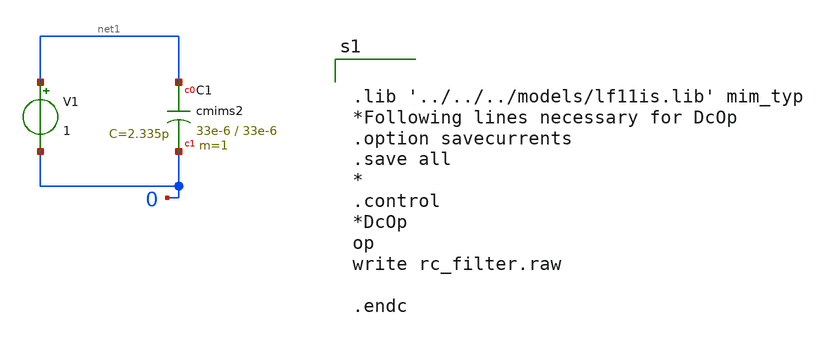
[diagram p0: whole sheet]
** sch_path: test_cmims2LF.sch
**.subckt test_cmims2LF
V1 net1 0 1
XC1 net1 0 cmims2 w=33e-6 l=33e-6 m=1
**** begin user architecture code


.lib '../../../models/lf11is.lib' mim_typ
*Following lines necessary for DcOp
.option savecurrents
.save all
*
.control
*DcOp
op
write rc_filter.raw

.endc


**** end user architecture code
**.ends
.end
